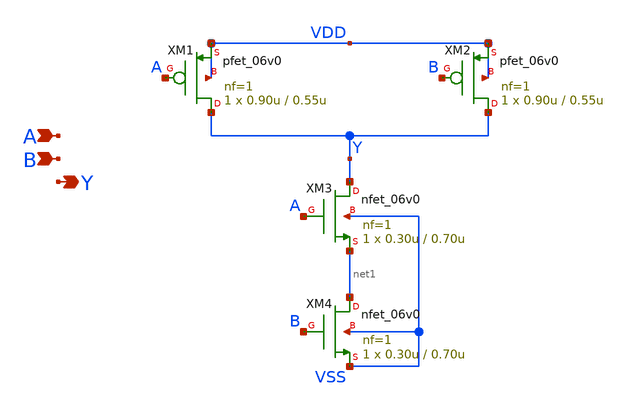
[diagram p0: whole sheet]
** sch_path: designs/libs/core_analog/digital/digital_nand2_1.sch
**.subckt digital_nand2_1 A B Y
*.ipin A
*.ipin B
*.opin Y
XM3 Y A net1 VSS nfet_06v0 L=0.70u W=0.30u nf=1 ad='int((nf+1)/2) * W/nf * 0.18u' as='int((nf+2)/2) * W/nf * 0.18u'
+ pd='2*int((nf+1)/2) * (W/nf + 0.18u)' ps='2*int((nf+2)/2) * (W/nf + 0.18u)' nrd='0.18u / W' nrs='0.18u / W'
+ sa=0 sb=0 sd=0 m=1
XM4 net1 B VSS VSS nfet_06v0 L=0.70u W=0.30u nf=1 ad='int((nf+1)/2) * W/nf * 0.18u' as='int((nf+2)/2) * W/nf * 0.18u'
+ pd='2*int((nf+1)/2) * (W/nf + 0.18u)' ps='2*int((nf+2)/2) * (W/nf + 0.18u)' nrd='0.18u / W' nrs='0.18u / W'
+ sa=0 sb=0 sd=0 m=1
XM1 Y A VDD VDD pfet_06v0 L=0.55u W=0.90u nf=1 ad='int((nf+1)/2) * W/nf * 0.18u' as='int((nf+2)/2) * W/nf * 0.18u'
+ pd='2*int((nf+1)/2) * (W/nf + 0.18u)' ps='2*int((nf+2)/2) * (W/nf + 0.18u)' nrd='0.18u / W' nrs='0.18u / W'
+ sa=0 sb=0 sd=0 m=1
XM2 Y B VDD VDD pfet_06v0 L=0.55u W=0.90u nf=1 ad='int((nf+1)/2) * W/nf * 0.18u' as='int((nf+2)/2) * W/nf * 0.18u'
+ pd='2*int((nf+1)/2) * (W/nf + 0.18u)' ps='2*int((nf+2)/2) * (W/nf + 0.18u)' nrd='0.18u / W' nrs='0.18u / W'
+ sa=0 sb=0 sd=0 m=1
**.ends
.end
